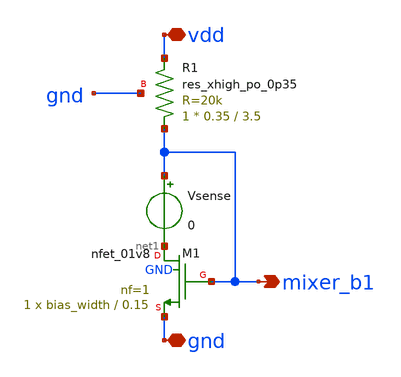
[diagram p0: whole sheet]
** sch_path: xschem/bias.sch
**.subckt bias vdd gnd mixer_b1
*.iopin vdd
*.iopin gnd
*.opin mixer_b1
XM1 net1 mixer_b1 gnd GND sky130_fd_pr__nfet_01v8 L=0.15 W=bias_width nf=1 ad='int((nf+1)/2) * W/nf * 0.29'
+ as='int((nf+2)/2) * W/nf * 0.29' pd='2*int((nf+1)/2) * (W/nf + 0.29)' ps='2*int((nf+2)/2) * (W/nf + 0.29)'
+ nrd='0.29 / W' nrs='0.29 / W' sa=0 sb=0 sd=0 mult=1 m=1
XR1 mixer_b1 vdd gnd sky130_fd_pr__res_xhigh_po_0p35 L=3.5 mult=1 m=1
Vsense mixer_b1 net1 0
**.ends
.end
